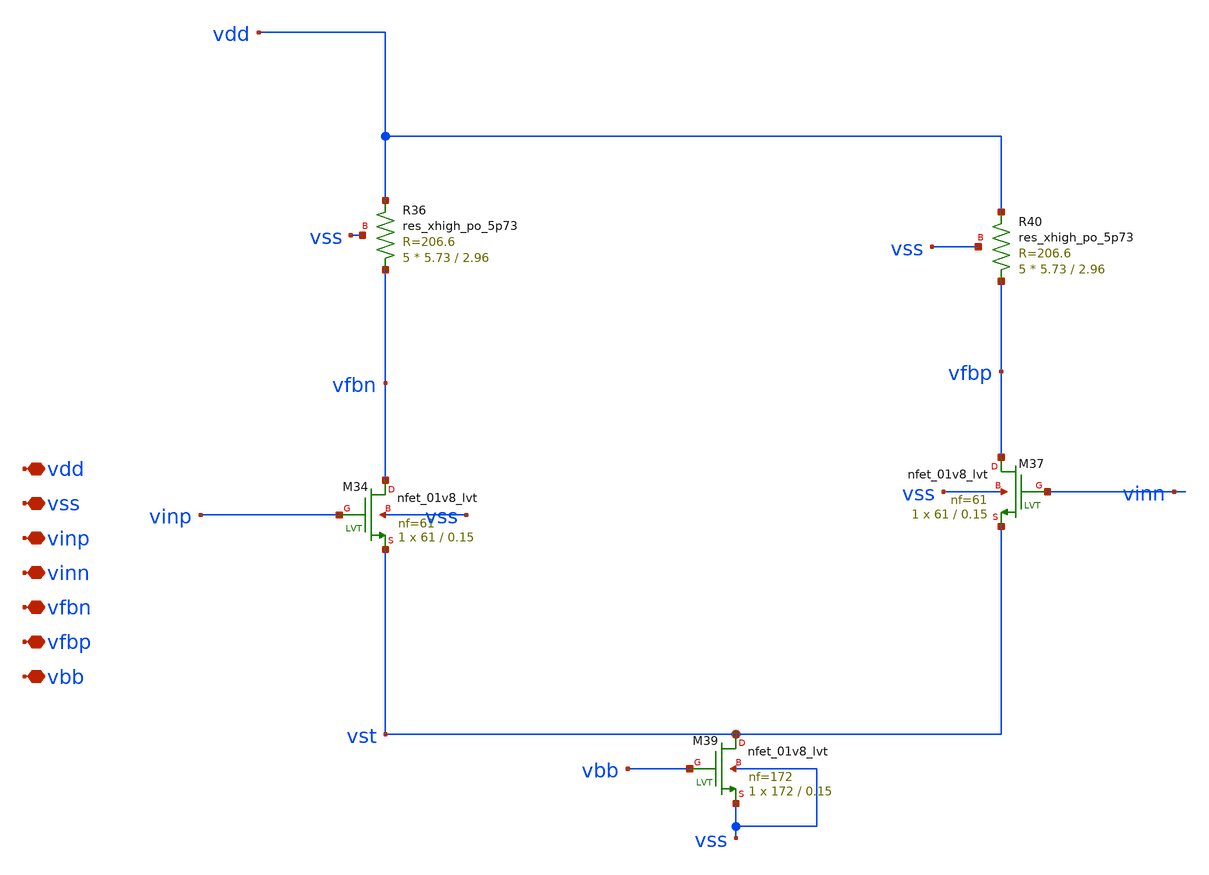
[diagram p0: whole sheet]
** sch_path: design/vga/buffer_os.sch
**.subckt buffer_os vdd vss vinp vinn vfbn vfbp vbb
*.iopin vdd
*.iopin vss
*.iopin vinp
*.iopin vinn
*.iopin vfbn
*.iopin vfbp
*.iopin vbb
XR36 vfbn vdd vss sky130_fd_pr__res_xhigh_po_5p73 L=2.96 mult=5 m=5
XR40 vfbp vdd vss sky130_fd_pr__res_xhigh_po_5p73 L=2.96 mult=5 m=5
XM34 vfbn vinp vst vss sky130_fd_pr__nfet_01v8_lvt L=0.15 W=61 nf=61 ad='int((nf+1)/2) * W/nf * 0.29'
+ as='int((nf+2)/2) * W/nf * 0.29' pd='2*int((nf+1)/2) * (W/nf + 0.29)' ps='2*int((nf+2)/2) * (W/nf + 0.29)'
+ nrd='0.29 / W' nrs='0.29 / W' sa=0 sb=0 sd=0 mult=1 m=1
XM37 vfbp vinn vst vss sky130_fd_pr__nfet_01v8_lvt L=0.15 W=61 nf=61 ad='int((nf+1)/2) * W/nf * 0.29'
+ as='int((nf+2)/2) * W/nf * 0.29' pd='2*int((nf+1)/2) * (W/nf + 0.29)' ps='2*int((nf+2)/2) * (W/nf + 0.29)'
+ nrd='0.29 / W' nrs='0.29 / W' sa=0 sb=0 sd=0 mult=1 m=1
XM39 vst vbb vss vss sky130_fd_pr__nfet_01v8_lvt L=0.15 W=172 nf=172 ad='int((nf+1)/2) * W/nf * 0.29'
+ as='int((nf+2)/2) * W/nf * 0.29' pd='2*int((nf+1)/2) * (W/nf + 0.29)' ps='2*int((nf+2)/2) * (W/nf + 0.29)'
+ nrd='0.29 / W' nrs='0.29 / W' sa=0 sb=0 sd=0 mult=1 m=1
**.ends
.end
